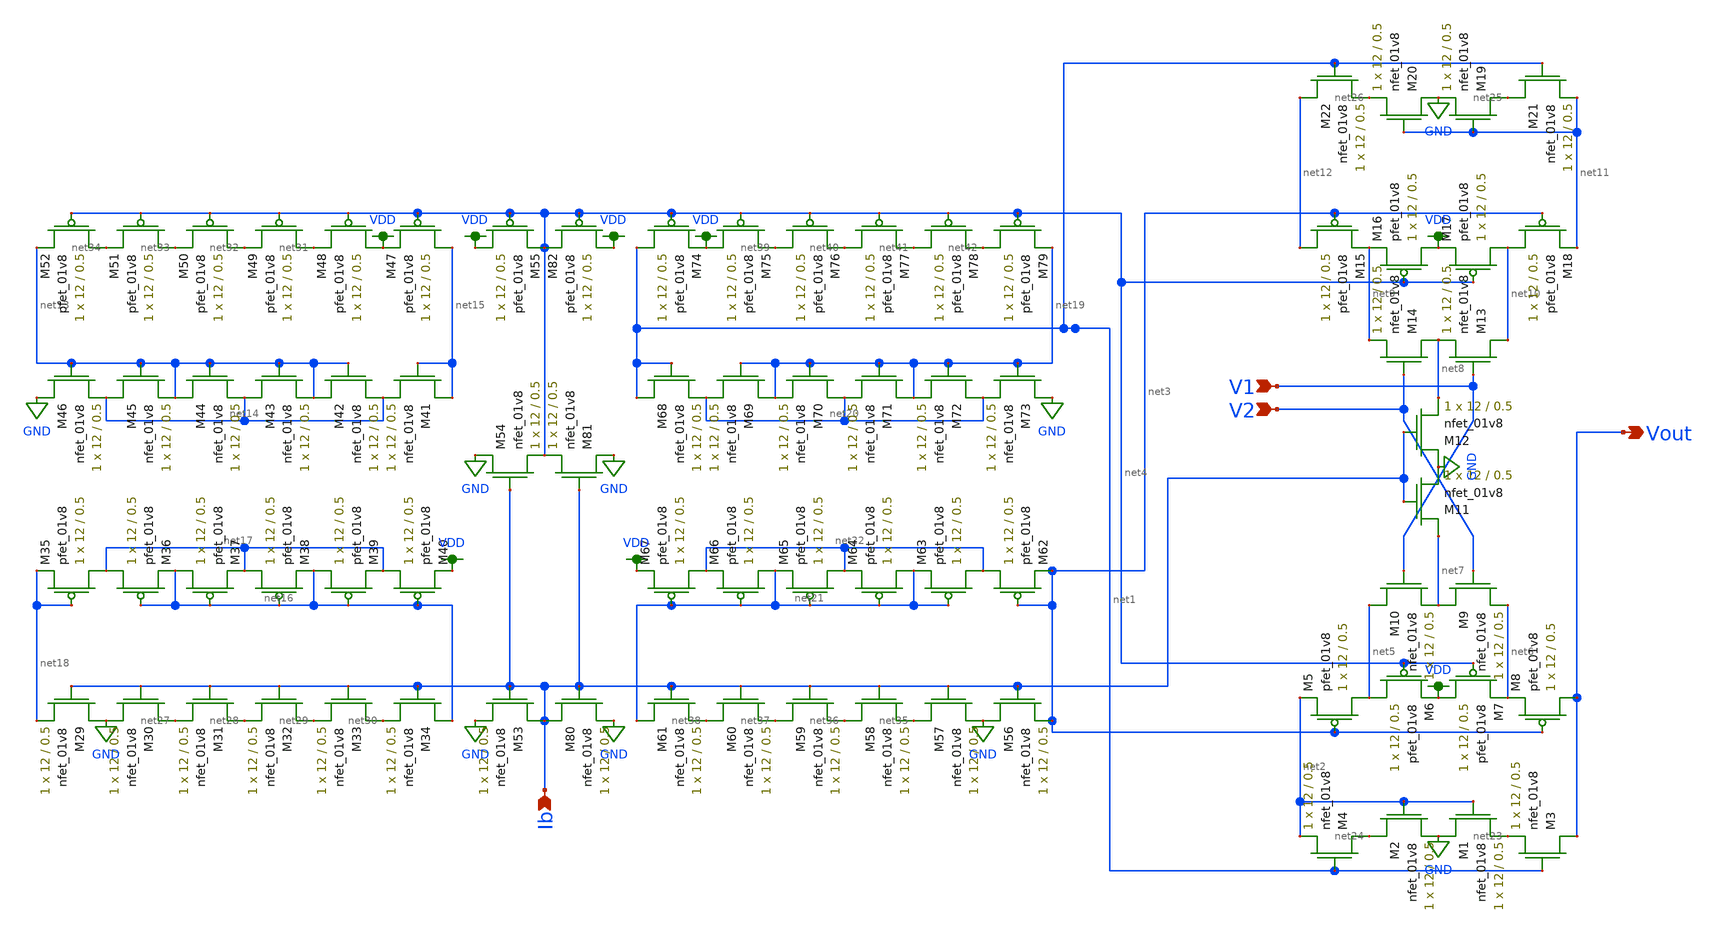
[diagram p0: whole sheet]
** sch_path: mp3/schematics/overall.sch
**.subckt overall V2 V1 Vout Ib
*.ipin V2
*.ipin V1
*.opin Vout
*.ipin Ib
XM1 GND net2 net23 GND sky130_fd_pr__nfet_01v8 L=0.5 W=12 nf=1 ad='int((nf+1)/2) * W/nf * 0.29' as='int((nf+2)/2) * W/nf * 0.29'
+ pd='2*int((nf+1)/2) * (W/nf + 0.29)' ps='2*int((nf+2)/2) * (W/nf + 0.29)' nrd='0.29 / W' nrs='0.29 / W'
+ sa=0 sb=0 sd=0 mult=1 m=1
XM2 net24 net2 GND GND sky130_fd_pr__nfet_01v8 L=0.5 W=12 nf=1 ad='int((nf+1)/2) * W/nf * 0.29' as='int((nf+2)/2) * W/nf * 0.29'
+ pd='2*int((nf+1)/2) * (W/nf + 0.29)' ps='2*int((nf+2)/2) * (W/nf + 0.29)' nrd='0.29 / W' nrs='0.29 / W'
+ sa=0 sb=0 sd=0 mult=1 m=1
XM3 Vout net1 net23 GND sky130_fd_pr__nfet_01v8 L=0.5 W=12 nf=1 ad='int((nf+1)/2) * W/nf * 0.29' as='int((nf+2)/2) * W/nf * 0.29'
+ pd='2*int((nf+1)/2) * (W/nf + 0.29)' ps='2*int((nf+2)/2) * (W/nf + 0.29)' nrd='0.29 / W' nrs='0.29 / W'
+ sa=0 sb=0 sd=0 mult=1 m=1
XM4 net24 net1 net2 GND sky130_fd_pr__nfet_01v8 L=0.5 W=12 nf=1 ad='int((nf+1)/2) * W/nf * 0.29' as='int((nf+2)/2) * W/nf * 0.29'
+ pd='2*int((nf+1)/2) * (W/nf + 0.29)' ps='2*int((nf+2)/2) * (W/nf + 0.29)' nrd='0.29 / W' nrs='0.29 / W'
+ sa=0 sb=0 sd=0 mult=1 m=1
XM5 net5 net3 net2 VDD sky130_fd_pr__pfet_01v8 L=0.5 W=12 nf=1 ad='int((nf+1)/2) * W/nf * 0.29' as='int((nf+2)/2) * W/nf * 0.29'
+ pd='2*int((nf+1)/2) * (W/nf + 0.29)' ps='2*int((nf+2)/2) * (W/nf + 0.29)' nrd='0.29 / W' nrs='0.29 / W'
+ sa=0 sb=0 sd=0 mult=1 m=1
XM6 net5 net4 VDD VDD sky130_fd_pr__pfet_01v8 L=0.5 W=12 nf=1 ad='int((nf+1)/2) * W/nf * 0.29' as='int((nf+2)/2) * W/nf * 0.29'
+ pd='2*int((nf+1)/2) * (W/nf + 0.29)' ps='2*int((nf+2)/2) * (W/nf + 0.29)' nrd='0.29 / W' nrs='0.29 / W'
+ sa=0 sb=0 sd=0 mult=1 m=1
XM7 VDD net4 net6 VDD sky130_fd_pr__pfet_01v8 L=0.5 W=12 nf=1 ad='int((nf+1)/2) * W/nf * 0.29' as='int((nf+2)/2) * W/nf * 0.29'
+ pd='2*int((nf+1)/2) * (W/nf + 0.29)' ps='2*int((nf+2)/2) * (W/nf + 0.29)' nrd='0.29 / W' nrs='0.29 / W'
+ sa=0 sb=0 sd=0 mult=1 m=1
XM8 Vout net3 net6 VDD sky130_fd_pr__pfet_01v8 L=0.5 W=12 nf=1 ad='int((nf+1)/2) * W/nf * 0.29' as='int((nf+2)/2) * W/nf * 0.29'
+ pd='2*int((nf+1)/2) * (W/nf + 0.29)' ps='2*int((nf+2)/2) * (W/nf + 0.29)' nrd='0.29 / W' nrs='0.29 / W'
+ sa=0 sb=0 sd=0 mult=1 m=1
XM9 net7 V2 net6 GND sky130_fd_pr__nfet_01v8 L=0.5 W=12 nf=1 ad='int((nf+1)/2) * W/nf * 0.29' as='int((nf+2)/2) * W/nf * 0.29'
+ pd='2*int((nf+1)/2) * (W/nf + 0.29)' ps='2*int((nf+2)/2) * (W/nf + 0.29)' nrd='0.29 / W' nrs='0.29 / W'
+ sa=0 sb=0 sd=0 mult=1 m=1
XM10 net5 V1 net7 GND sky130_fd_pr__nfet_01v8 L=0.5 W=12 nf=1 ad='int((nf+1)/2) * W/nf * 0.29' as='int((nf+2)/2) * W/nf * 0.29'
+ pd='2*int((nf+1)/2) * (W/nf + 0.29)' ps='2*int((nf+2)/2) * (W/nf + 0.29)' nrd='0.29 / W' nrs='0.29 / W'
+ sa=0 sb=0 sd=0 mult=1 m=1
XM11 net7 Ib GND GND sky130_fd_pr__nfet_01v8 L=0.5 W=12 nf=1 ad='int((nf+1)/2) * W/nf * 0.29' as='int((nf+2)/2) * W/nf * 0.29'
+ pd='2*int((nf+1)/2) * (W/nf + 0.29)' ps='2*int((nf+2)/2) * (W/nf + 0.29)' nrd='0.29 / W' nrs='0.29 / W'
+ sa=0 sb=0 sd=0 mult=1 m=1
XM12 GND Ib net8 GND sky130_fd_pr__nfet_01v8 L=0.5 W=12 nf=1 ad='int((nf+1)/2) * W/nf * 0.29' as='int((nf+2)/2) * W/nf * 0.29'
+ pd='2*int((nf+1)/2) * (W/nf + 0.29)' ps='2*int((nf+2)/2) * (W/nf + 0.29)' nrd='0.29 / W' nrs='0.29 / W'
+ sa=0 sb=0 sd=0 mult=1 m=1
XM13 net10 V1 net8 GND sky130_fd_pr__nfet_01v8 L=0.5 W=12 nf=1 ad='int((nf+1)/2) * W/nf * 0.29' as='int((nf+2)/2) * W/nf * 0.29'
+ pd='2*int((nf+1)/2) * (W/nf + 0.29)' ps='2*int((nf+2)/2) * (W/nf + 0.29)' nrd='0.29 / W' nrs='0.29 / W'
+ sa=0 sb=0 sd=0 mult=1 m=1
XM14 net8 V2 net9 GND sky130_fd_pr__nfet_01v8 L=0.5 W=12 nf=1 ad='int((nf+1)/2) * W/nf * 0.29' as='int((nf+2)/2) * W/nf * 0.29'
+ pd='2*int((nf+1)/2) * (W/nf + 0.29)' ps='2*int((nf+2)/2) * (W/nf + 0.29)' nrd='0.29 / W' nrs='0.29 / W'
+ sa=0 sb=0 sd=0 mult=1 m=1
XM15 net12 net3 net9 VDD sky130_fd_pr__pfet_01v8 L=0.5 W=12 nf=1 ad='int((nf+1)/2) * W/nf * 0.29' as='int((nf+2)/2) * W/nf * 0.29'
+ pd='2*int((nf+1)/2) * (W/nf + 0.29)' ps='2*int((nf+2)/2) * (W/nf + 0.29)' nrd='0.29 / W' nrs='0.29 / W'
+ sa=0 sb=0 sd=0 mult=1 m=1
XM16 VDD net4 net9 VDD sky130_fd_pr__pfet_01v8 L=0.5 W=12 nf=1 ad='int((nf+1)/2) * W/nf * 0.29' as='int((nf+2)/2) * W/nf * 0.29'
+ pd='2*int((nf+1)/2) * (W/nf + 0.29)' ps='2*int((nf+2)/2) * (W/nf + 0.29)' nrd='0.29 / W' nrs='0.29 / W'
+ sa=0 sb=0 sd=0 mult=1 m=1
XM17 net10 net4 VDD VDD sky130_fd_pr__pfet_01v8 L=0.5 W=12 nf=1 ad='int((nf+1)/2) * W/nf * 0.29' as='int((nf+2)/2) * W/nf * 0.29'
+ pd='2*int((nf+1)/2) * (W/nf + 0.29)' ps='2*int((nf+2)/2) * (W/nf + 0.29)' nrd='0.29 / W' nrs='0.29 / W'
+ sa=0 sb=0 sd=0 mult=1 m=1
XM18 net10 net3 net11 VDD sky130_fd_pr__pfet_01v8 L=0.5 W=12 nf=1 ad='int((nf+1)/2) * W/nf * 0.29' as='int((nf+2)/2) * W/nf * 0.29'
+ pd='2*int((nf+1)/2) * (W/nf + 0.29)' ps='2*int((nf+2)/2) * (W/nf + 0.29)' nrd='0.29 / W' nrs='0.29 / W'
+ sa=0 sb=0 sd=0 mult=1 m=1
XM19 net25 net11 GND GND sky130_fd_pr__nfet_01v8 L=0.5 W=12 nf=1 ad='int((nf+1)/2) * W/nf * 0.29' as='int((nf+2)/2) * W/nf * 0.29'
+ pd='2*int((nf+1)/2) * (W/nf + 0.29)' ps='2*int((nf+2)/2) * (W/nf + 0.29)' nrd='0.29 / W' nrs='0.29 / W'
+ sa=0 sb=0 sd=0 mult=1 m=1
XM20 GND net11 net26 GND sky130_fd_pr__nfet_01v8 L=0.5 W=12 nf=1 ad='int((nf+1)/2) * W/nf * 0.29' as='int((nf+2)/2) * W/nf * 0.29'
+ pd='2*int((nf+1)/2) * (W/nf + 0.29)' ps='2*int((nf+2)/2) * (W/nf + 0.29)' nrd='0.29 / W' nrs='0.29 / W'
+ sa=0 sb=0 sd=0 mult=1 m=1
XM21 net25 net1 net11 GND sky130_fd_pr__nfet_01v8 L=0.5 W=12 nf=1 ad='int((nf+1)/2) * W/nf * 0.29' as='int((nf+2)/2) * W/nf * 0.29'
+ pd='2*int((nf+1)/2) * (W/nf + 0.29)' ps='2*int((nf+2)/2) * (W/nf + 0.29)' nrd='0.29 / W' nrs='0.29 / W'
+ sa=0 sb=0 sd=0 mult=1 m=1
XM22 net12 net1 net26 GND sky130_fd_pr__nfet_01v8 L=0.5 W=12 nf=1 ad='int((nf+1)/2) * W/nf * 0.29' as='int((nf+2)/2) * W/nf * 0.29'
+ pd='2*int((nf+1)/2) * (W/nf + 0.29)' ps='2*int((nf+2)/2) * (W/nf + 0.29)' nrd='0.29 / W' nrs='0.29 / W'
+ sa=0 sb=0 sd=0 mult=1 m=1
XM29 GND Ib net18 GND sky130_fd_pr__nfet_01v8 L=0.5 W=12 nf=1 ad='int((nf+1)/2) * W/nf * 0.29' as='int((nf+2)/2) * W/nf * 0.29'
+ pd='2*int((nf+1)/2) * (W/nf + 0.29)' ps='2*int((nf+2)/2) * (W/nf + 0.29)' nrd='0.29 / W' nrs='0.29 / W'
+ sa=0 sb=0 sd=0 mult=1 m=1
XM30 net27 Ib GND GND sky130_fd_pr__nfet_01v8 L=0.5 W=12 nf=1 ad='int((nf+1)/2) * W/nf * 0.29' as='int((nf+2)/2) * W/nf * 0.29'
+ pd='2*int((nf+1)/2) * (W/nf + 0.29)' ps='2*int((nf+2)/2) * (W/nf + 0.29)' nrd='0.29 / W' nrs='0.29 / W'
+ sa=0 sb=0 sd=0 mult=1 m=1
XM31 net28 Ib net27 GND sky130_fd_pr__nfet_01v8 L=0.5 W=12 nf=1 ad='int((nf+1)/2) * W/nf * 0.29' as='int((nf+2)/2) * W/nf * 0.29'
+ pd='2*int((nf+1)/2) * (W/nf + 0.29)' ps='2*int((nf+2)/2) * (W/nf + 0.29)' nrd='0.29 / W' nrs='0.29 / W'
+ sa=0 sb=0 sd=0 mult=1 m=1
XM32 net29 Ib net28 GND sky130_fd_pr__nfet_01v8 L=0.5 W=12 nf=1 ad='int((nf+1)/2) * W/nf * 0.29' as='int((nf+2)/2) * W/nf * 0.29'
+ pd='2*int((nf+1)/2) * (W/nf + 0.29)' ps='2*int((nf+2)/2) * (W/nf + 0.29)' nrd='0.29 / W' nrs='0.29 / W'
+ sa=0 sb=0 sd=0 mult=1 m=1
XM33 net30 Ib net29 GND sky130_fd_pr__nfet_01v8 L=0.5 W=12 nf=1 ad='int((nf+1)/2) * W/nf * 0.29' as='int((nf+2)/2) * W/nf * 0.29'
+ pd='2*int((nf+1)/2) * (W/nf + 0.29)' ps='2*int((nf+2)/2) * (W/nf + 0.29)' nrd='0.29 / W' nrs='0.29 / W'
+ sa=0 sb=0 sd=0 mult=1 m=1
XM34 net16 Ib net30 GND sky130_fd_pr__nfet_01v8 L=0.5 W=12 nf=1 ad='int((nf+1)/2) * W/nf * 0.29' as='int((nf+2)/2) * W/nf * 0.29'
+ pd='2*int((nf+1)/2) * (W/nf + 0.29)' ps='2*int((nf+2)/2) * (W/nf + 0.29)' nrd='0.29 / W' nrs='0.29 / W'
+ sa=0 sb=0 sd=0 mult=1 m=1
XM35 net17 net18 net18 VDD sky130_fd_pr__pfet_01v8 L=0.5 W=12 nf=1 ad='int((nf+1)/2) * W/nf * 0.29' as='int((nf+2)/2) * W/nf * 0.29'
+ pd='2*int((nf+1)/2) * (W/nf + 0.29)' ps='2*int((nf+2)/2) * (W/nf + 0.29)' nrd='0.29 / W' nrs='0.29 / W'
+ sa=0 sb=0 sd=0 mult=1 m=1
XM36 net17 net16 net16 VDD sky130_fd_pr__pfet_01v8 L=0.5 W=12 nf=1 ad='int((nf+1)/2) * W/nf * 0.29' as='int((nf+2)/2) * W/nf * 0.29'
+ pd='2*int((nf+1)/2) * (W/nf + 0.29)' ps='2*int((nf+2)/2) * (W/nf + 0.29)' nrd='0.29 / W' nrs='0.29 / W'
+ sa=0 sb=0 sd=0 mult=1 m=1
XM37 net16 net16 net17 VDD sky130_fd_pr__pfet_01v8 L=0.5 W=12 nf=1 ad='int((nf+1)/2) * W/nf * 0.29' as='int((nf+2)/2) * W/nf * 0.29'
+ pd='2*int((nf+1)/2) * (W/nf + 0.29)' ps='2*int((nf+2)/2) * (W/nf + 0.29)' nrd='0.29 / W' nrs='0.29 / W'
+ sa=0 sb=0 sd=0 mult=1 m=1
XM38 net17 net16 net16 VDD sky130_fd_pr__pfet_01v8 L=0.5 W=12 nf=1 ad='int((nf+1)/2) * W/nf * 0.29' as='int((nf+2)/2) * W/nf * 0.29'
+ pd='2*int((nf+1)/2) * (W/nf + 0.29)' ps='2*int((nf+2)/2) * (W/nf + 0.29)' nrd='0.29 / W' nrs='0.29 / W'
+ sa=0 sb=0 sd=0 mult=1 m=1
XM39 net16 net16 net17 VDD sky130_fd_pr__pfet_01v8 L=0.5 W=12 nf=1 ad='int((nf+1)/2) * W/nf * 0.29' as='int((nf+2)/2) * W/nf * 0.29'
+ pd='2*int((nf+1)/2) * (W/nf + 0.29)' ps='2*int((nf+2)/2) * (W/nf + 0.29)' nrd='0.29 / W' nrs='0.29 / W'
+ sa=0 sb=0 sd=0 mult=1 m=1
XM40 net17 net16 VDD VDD sky130_fd_pr__pfet_01v8 L=0.5 W=12 nf=1 ad='int((nf+1)/2) * W/nf * 0.29' as='int((nf+2)/2) * W/nf * 0.29'
+ pd='2*int((nf+1)/2) * (W/nf + 0.29)' ps='2*int((nf+2)/2) * (W/nf + 0.29)' nrd='0.29 / W' nrs='0.29 / W'
+ sa=0 sb=0 sd=0 mult=1 m=1
XM41 net15 net15 net14 GND sky130_fd_pr__nfet_01v8 L=0.5 W=12 nf=1 ad='int((nf+1)/2) * W/nf * 0.29' as='int((nf+2)/2) * W/nf * 0.29'
+ pd='2*int((nf+1)/2) * (W/nf + 0.29)' ps='2*int((nf+2)/2) * (W/nf + 0.29)' nrd='0.29 / W' nrs='0.29 / W'
+ sa=0 sb=0 sd=0 mult=1 m=1
XM42 net13 net13 net14 GND sky130_fd_pr__nfet_01v8 L=0.5 W=12 nf=1 ad='int((nf+1)/2) * W/nf * 0.29' as='int((nf+2)/2) * W/nf * 0.29'
+ pd='2*int((nf+1)/2) * (W/nf + 0.29)' ps='2*int((nf+2)/2) * (W/nf + 0.29)' nrd='0.29 / W' nrs='0.29 / W'
+ sa=0 sb=0 sd=0 mult=1 m=1
XM43 net14 net13 net13 GND sky130_fd_pr__nfet_01v8 L=0.5 W=12 nf=1 ad='int((nf+1)/2) * W/nf * 0.29' as='int((nf+2)/2) * W/nf * 0.29'
+ pd='2*int((nf+1)/2) * (W/nf + 0.29)' ps='2*int((nf+2)/2) * (W/nf + 0.29)' nrd='0.29 / W' nrs='0.29 / W'
+ sa=0 sb=0 sd=0 mult=1 m=1
XM44 net13 net13 net14 GND sky130_fd_pr__nfet_01v8 L=0.5 W=12 nf=1 ad='int((nf+1)/2) * W/nf * 0.29' as='int((nf+2)/2) * W/nf * 0.29'
+ pd='2*int((nf+1)/2) * (W/nf + 0.29)' ps='2*int((nf+2)/2) * (W/nf + 0.29)' nrd='0.29 / W' nrs='0.29 / W'
+ sa=0 sb=0 sd=0 mult=1 m=1
XM45 net14 net13 net13 GND sky130_fd_pr__nfet_01v8 L=0.5 W=12 nf=1 ad='int((nf+1)/2) * W/nf * 0.29' as='int((nf+2)/2) * W/nf * 0.29'
+ pd='2*int((nf+1)/2) * (W/nf + 0.29)' ps='2*int((nf+2)/2) * (W/nf + 0.29)' nrd='0.29 / W' nrs='0.29 / W'
+ sa=0 sb=0 sd=0 mult=1 m=1
XM46 GND net13 net14 GND sky130_fd_pr__nfet_01v8 L=0.5 W=12 nf=1 ad='int((nf+1)/2) * W/nf * 0.29' as='int((nf+2)/2) * W/nf * 0.29'
+ pd='2*int((nf+1)/2) * (W/nf + 0.29)' ps='2*int((nf+2)/2) * (W/nf + 0.29)' nrd='0.29 / W' nrs='0.29 / W'
+ sa=0 sb=0 sd=0 mult=1 m=1
XM47 net15 net4 VDD VDD sky130_fd_pr__pfet_01v8 L=0.5 W=12 nf=1 ad='int((nf+1)/2) * W/nf * 0.29' as='int((nf+2)/2) * W/nf * 0.29'
+ pd='2*int((nf+1)/2) * (W/nf + 0.29)' ps='2*int((nf+2)/2) * (W/nf + 0.29)' nrd='0.29 / W' nrs='0.29 / W'
+ sa=0 sb=0 sd=0 mult=1 m=1
XM48 VDD net4 net31 VDD sky130_fd_pr__pfet_01v8 L=0.5 W=12 nf=1 ad='int((nf+1)/2) * W/nf * 0.29' as='int((nf+2)/2) * W/nf * 0.29'
+ pd='2*int((nf+1)/2) * (W/nf + 0.29)' ps='2*int((nf+2)/2) * (W/nf + 0.29)' nrd='0.29 / W' nrs='0.29 / W'
+ sa=0 sb=0 sd=0 mult=1 m=1
XM49 net31 net4 net32 VDD sky130_fd_pr__pfet_01v8 L=0.5 W=12 nf=1 ad='int((nf+1)/2) * W/nf * 0.29' as='int((nf+2)/2) * W/nf * 0.29'
+ pd='2*int((nf+1)/2) * (W/nf + 0.29)' ps='2*int((nf+2)/2) * (W/nf + 0.29)' nrd='0.29 / W' nrs='0.29 / W'
+ sa=0 sb=0 sd=0 mult=1 m=1
XM50 net32 net4 net33 VDD sky130_fd_pr__pfet_01v8 L=0.5 W=12 nf=1 ad='int((nf+1)/2) * W/nf * 0.29' as='int((nf+2)/2) * W/nf * 0.29'
+ pd='2*int((nf+1)/2) * (W/nf + 0.29)' ps='2*int((nf+2)/2) * (W/nf + 0.29)' nrd='0.29 / W' nrs='0.29 / W'
+ sa=0 sb=0 sd=0 mult=1 m=1
XM51 net33 net4 net34 VDD sky130_fd_pr__pfet_01v8 L=0.5 W=12 nf=1 ad='int((nf+1)/2) * W/nf * 0.29' as='int((nf+2)/2) * W/nf * 0.29'
+ pd='2*int((nf+1)/2) * (W/nf + 0.29)' ps='2*int((nf+2)/2) * (W/nf + 0.29)' nrd='0.29 / W' nrs='0.29 / W'
+ sa=0 sb=0 sd=0 mult=1 m=1
XM52 net34 net4 net13 VDD sky130_fd_pr__pfet_01v8 L=0.5 W=12 nf=1 ad='int((nf+1)/2) * W/nf * 0.29' as='int((nf+2)/2) * W/nf * 0.29'
+ pd='2*int((nf+1)/2) * (W/nf + 0.29)' ps='2*int((nf+2)/2) * (W/nf + 0.29)' nrd='0.29 / W' nrs='0.29 / W'
+ sa=0 sb=0 sd=0 mult=1 m=1
XM53 Ib Ib GND GND sky130_fd_pr__nfet_01v8 L=0.5 W=12 nf=1 ad='int((nf+1)/2) * W/nf * 0.29' as='int((nf+2)/2) * W/nf * 0.29'
+ pd='2*int((nf+1)/2) * (W/nf + 0.29)' ps='2*int((nf+2)/2) * (W/nf + 0.29)' nrd='0.29 / W' nrs='0.29 / W'
+ sa=0 sb=0 sd=0 mult=1 m=1
XM54 GND Ib net4 GND sky130_fd_pr__nfet_01v8 L=0.5 W=12 nf=1 ad='int((nf+1)/2) * W/nf * 0.29' as='int((nf+2)/2) * W/nf * 0.29'
+ pd='2*int((nf+1)/2) * (W/nf + 0.29)' ps='2*int((nf+2)/2) * (W/nf + 0.29)' nrd='0.29 / W' nrs='0.29 / W'
+ sa=0 sb=0 sd=0 mult=1 m=1
XM55 VDD net4 net4 VDD sky130_fd_pr__pfet_01v8 L=0.5 W=12 nf=1 ad='int((nf+1)/2) * W/nf * 0.29' as='int((nf+2)/2) * W/nf * 0.29'
+ pd='2*int((nf+1)/2) * (W/nf + 0.29)' ps='2*int((nf+2)/2) * (W/nf + 0.29)' nrd='0.29 / W' nrs='0.29 / W'
+ sa=0 sb=0 sd=0 mult=1 m=1
XM56 GND Ib net3 GND sky130_fd_pr__nfet_01v8 L=0.5 W=12 nf=1 ad='int((nf+1)/2) * W/nf * 0.29' as='int((nf+2)/2) * W/nf * 0.29'
+ pd='2*int((nf+1)/2) * (W/nf + 0.29)' ps='2*int((nf+2)/2) * (W/nf + 0.29)' nrd='0.29 / W' nrs='0.29 / W'
+ sa=0 sb=0 sd=0 mult=1 m=1
XM57 net35 Ib GND GND sky130_fd_pr__nfet_01v8 L=0.5 W=12 nf=1 ad='int((nf+1)/2) * W/nf * 0.29' as='int((nf+2)/2) * W/nf * 0.29'
+ pd='2*int((nf+1)/2) * (W/nf + 0.29)' ps='2*int((nf+2)/2) * (W/nf + 0.29)' nrd='0.29 / W' nrs='0.29 / W'
+ sa=0 sb=0 sd=0 mult=1 m=1
XM58 net36 Ib net35 GND sky130_fd_pr__nfet_01v8 L=0.5 W=12 nf=1 ad='int((nf+1)/2) * W/nf * 0.29' as='int((nf+2)/2) * W/nf * 0.29'
+ pd='2*int((nf+1)/2) * (W/nf + 0.29)' ps='2*int((nf+2)/2) * (W/nf + 0.29)' nrd='0.29 / W' nrs='0.29 / W'
+ sa=0 sb=0 sd=0 mult=1 m=1
XM59 net37 Ib net36 GND sky130_fd_pr__nfet_01v8 L=0.5 W=12 nf=1 ad='int((nf+1)/2) * W/nf * 0.29' as='int((nf+2)/2) * W/nf * 0.29'
+ pd='2*int((nf+1)/2) * (W/nf + 0.29)' ps='2*int((nf+2)/2) * (W/nf + 0.29)' nrd='0.29 / W' nrs='0.29 / W'
+ sa=0 sb=0 sd=0 mult=1 m=1
XM60 net38 Ib net37 GND sky130_fd_pr__nfet_01v8 L=0.5 W=12 nf=1 ad='int((nf+1)/2) * W/nf * 0.29' as='int((nf+2)/2) * W/nf * 0.29'
+ pd='2*int((nf+1)/2) * (W/nf + 0.29)' ps='2*int((nf+2)/2) * (W/nf + 0.29)' nrd='0.29 / W' nrs='0.29 / W'
+ sa=0 sb=0 sd=0 mult=1 m=1
XM61 net21 Ib net38 GND sky130_fd_pr__nfet_01v8 L=0.5 W=12 nf=1 ad='int((nf+1)/2) * W/nf * 0.29' as='int((nf+2)/2) * W/nf * 0.29'
+ pd='2*int((nf+1)/2) * (W/nf + 0.29)' ps='2*int((nf+2)/2) * (W/nf + 0.29)' nrd='0.29 / W' nrs='0.29 / W'
+ sa=0 sb=0 sd=0 mult=1 m=1
XM62 net22 net3 net3 VDD sky130_fd_pr__pfet_01v8 L=0.5 W=12 nf=1 ad='int((nf+1)/2) * W/nf * 0.29' as='int((nf+2)/2) * W/nf * 0.29'
+ pd='2*int((nf+1)/2) * (W/nf + 0.29)' ps='2*int((nf+2)/2) * (W/nf + 0.29)' nrd='0.29 / W' nrs='0.29 / W'
+ sa=0 sb=0 sd=0 mult=1 m=1
XM63 net22 net21 net21 VDD sky130_fd_pr__pfet_01v8 L=0.5 W=12 nf=1 ad='int((nf+1)/2) * W/nf * 0.29' as='int((nf+2)/2) * W/nf * 0.29'
+ pd='2*int((nf+1)/2) * (W/nf + 0.29)' ps='2*int((nf+2)/2) * (W/nf + 0.29)' nrd='0.29 / W' nrs='0.29 / W'
+ sa=0 sb=0 sd=0 mult=1 m=1
XM64 net21 net21 net22 VDD sky130_fd_pr__pfet_01v8 L=0.5 W=12 nf=1 ad='int((nf+1)/2) * W/nf * 0.29' as='int((nf+2)/2) * W/nf * 0.29'
+ pd='2*int((nf+1)/2) * (W/nf + 0.29)' ps='2*int((nf+2)/2) * (W/nf + 0.29)' nrd='0.29 / W' nrs='0.29 / W'
+ sa=0 sb=0 sd=0 mult=1 m=1
XM65 net22 net21 net21 VDD sky130_fd_pr__pfet_01v8 L=0.5 W=12 nf=1 ad='int((nf+1)/2) * W/nf * 0.29' as='int((nf+2)/2) * W/nf * 0.29'
+ pd='2*int((nf+1)/2) * (W/nf + 0.29)' ps='2*int((nf+2)/2) * (W/nf + 0.29)' nrd='0.29 / W' nrs='0.29 / W'
+ sa=0 sb=0 sd=0 mult=1 m=1
XM66 net21 net21 net22 VDD sky130_fd_pr__pfet_01v8 L=0.5 W=12 nf=1 ad='int((nf+1)/2) * W/nf * 0.29' as='int((nf+2)/2) * W/nf * 0.29'
+ pd='2*int((nf+1)/2) * (W/nf + 0.29)' ps='2*int((nf+2)/2) * (W/nf + 0.29)' nrd='0.29 / W' nrs='0.29 / W'
+ sa=0 sb=0 sd=0 mult=1 m=1
XM67 net22 net21 VDD VDD sky130_fd_pr__pfet_01v8 L=0.5 W=12 nf=1 ad='int((nf+1)/2) * W/nf * 0.29' as='int((nf+2)/2) * W/nf * 0.29'
+ pd='2*int((nf+1)/2) * (W/nf + 0.29)' ps='2*int((nf+2)/2) * (W/nf + 0.29)' nrd='0.29 / W' nrs='0.29 / W'
+ sa=0 sb=0 sd=0 mult=1 m=1
XM68 net1 net1 net20 GND sky130_fd_pr__nfet_01v8 L=0.5 W=12 nf=1 ad='int((nf+1)/2) * W/nf * 0.29' as='int((nf+2)/2) * W/nf * 0.29'
+ pd='2*int((nf+1)/2) * (W/nf + 0.29)' ps='2*int((nf+2)/2) * (W/nf + 0.29)' nrd='0.29 / W' nrs='0.29 / W'
+ sa=0 sb=0 sd=0 mult=1 m=1
XM69 net19 net19 net20 GND sky130_fd_pr__nfet_01v8 L=0.5 W=12 nf=1 ad='int((nf+1)/2) * W/nf * 0.29' as='int((nf+2)/2) * W/nf * 0.29'
+ pd='2*int((nf+1)/2) * (W/nf + 0.29)' ps='2*int((nf+2)/2) * (W/nf + 0.29)' nrd='0.29 / W' nrs='0.29 / W'
+ sa=0 sb=0 sd=0 mult=1 m=1
XM70 net20 net19 net19 GND sky130_fd_pr__nfet_01v8 L=0.5 W=12 nf=1 ad='int((nf+1)/2) * W/nf * 0.29' as='int((nf+2)/2) * W/nf * 0.29'
+ pd='2*int((nf+1)/2) * (W/nf + 0.29)' ps='2*int((nf+2)/2) * (W/nf + 0.29)' nrd='0.29 / W' nrs='0.29 / W'
+ sa=0 sb=0 sd=0 mult=1 m=1
XM71 net19 net19 net20 GND sky130_fd_pr__nfet_01v8 L=0.5 W=12 nf=1 ad='int((nf+1)/2) * W/nf * 0.29' as='int((nf+2)/2) * W/nf * 0.29'
+ pd='2*int((nf+1)/2) * (W/nf + 0.29)' ps='2*int((nf+2)/2) * (W/nf + 0.29)' nrd='0.29 / W' nrs='0.29 / W'
+ sa=0 sb=0 sd=0 mult=1 m=1
XM72 net20 net19 net19 GND sky130_fd_pr__nfet_01v8 L=0.5 W=12 nf=1 ad='int((nf+1)/2) * W/nf * 0.29' as='int((nf+2)/2) * W/nf * 0.29'
+ pd='2*int((nf+1)/2) * (W/nf + 0.29)' ps='2*int((nf+2)/2) * (W/nf + 0.29)' nrd='0.29 / W' nrs='0.29 / W'
+ sa=0 sb=0 sd=0 mult=1 m=1
XM73 GND net19 net20 GND sky130_fd_pr__nfet_01v8 L=0.5 W=12 nf=1 ad='int((nf+1)/2) * W/nf * 0.29' as='int((nf+2)/2) * W/nf * 0.29'
+ pd='2*int((nf+1)/2) * (W/nf + 0.29)' ps='2*int((nf+2)/2) * (W/nf + 0.29)' nrd='0.29 / W' nrs='0.29 / W'
+ sa=0 sb=0 sd=0 mult=1 m=1
XM74 net1 net4 VDD VDD sky130_fd_pr__pfet_01v8 L=0.5 W=12 nf=1 ad='int((nf+1)/2) * W/nf * 0.29' as='int((nf+2)/2) * W/nf * 0.29'
+ pd='2*int((nf+1)/2) * (W/nf + 0.29)' ps='2*int((nf+2)/2) * (W/nf + 0.29)' nrd='0.29 / W' nrs='0.29 / W'
+ sa=0 sb=0 sd=0 mult=1 m=1
XM75 VDD net4 net39 VDD sky130_fd_pr__pfet_01v8 L=0.5 W=12 nf=1 ad='int((nf+1)/2) * W/nf * 0.29' as='int((nf+2)/2) * W/nf * 0.29'
+ pd='2*int((nf+1)/2) * (W/nf + 0.29)' ps='2*int((nf+2)/2) * (W/nf + 0.29)' nrd='0.29 / W' nrs='0.29 / W'
+ sa=0 sb=0 sd=0 mult=1 m=1
XM76 net39 net4 net40 VDD sky130_fd_pr__pfet_01v8 L=0.5 W=12 nf=1 ad='int((nf+1)/2) * W/nf * 0.29' as='int((nf+2)/2) * W/nf * 0.29'
+ pd='2*int((nf+1)/2) * (W/nf + 0.29)' ps='2*int((nf+2)/2) * (W/nf + 0.29)' nrd='0.29 / W' nrs='0.29 / W'
+ sa=0 sb=0 sd=0 mult=1 m=1
XM77 net40 net4 net41 VDD sky130_fd_pr__pfet_01v8 L=0.5 W=12 nf=1 ad='int((nf+1)/2) * W/nf * 0.29' as='int((nf+2)/2) * W/nf * 0.29'
+ pd='2*int((nf+1)/2) * (W/nf + 0.29)' ps='2*int((nf+2)/2) * (W/nf + 0.29)' nrd='0.29 / W' nrs='0.29 / W'
+ sa=0 sb=0 sd=0 mult=1 m=1
XM78 net41 net4 net42 VDD sky130_fd_pr__pfet_01v8 L=0.5 W=12 nf=1 ad='int((nf+1)/2) * W/nf * 0.29' as='int((nf+2)/2) * W/nf * 0.29'
+ pd='2*int((nf+1)/2) * (W/nf + 0.29)' ps='2*int((nf+2)/2) * (W/nf + 0.29)' nrd='0.29 / W' nrs='0.29 / W'
+ sa=0 sb=0 sd=0 mult=1 m=1
XM79 net42 net4 net19 VDD sky130_fd_pr__pfet_01v8 L=0.5 W=12 nf=1 ad='int((nf+1)/2) * W/nf * 0.29' as='int((nf+2)/2) * W/nf * 0.29'
+ pd='2*int((nf+1)/2) * (W/nf + 0.29)' ps='2*int((nf+2)/2) * (W/nf + 0.29)' nrd='0.29 / W' nrs='0.29 / W'
+ sa=0 sb=0 sd=0 mult=1 m=1
XM80 Ib Ib GND GND sky130_fd_pr__nfet_01v8 L=0.5 W=12 nf=1 ad='int((nf+1)/2) * W/nf * 0.29' as='int((nf+2)/2) * W/nf * 0.29'
+ pd='2*int((nf+1)/2) * (W/nf + 0.29)' ps='2*int((nf+2)/2) * (W/nf + 0.29)' nrd='0.29 / W' nrs='0.29 / W'
+ sa=0 sb=0 sd=0 mult=1 m=1
XM81 GND Ib net4 GND sky130_fd_pr__nfet_01v8 L=0.5 W=12 nf=1 ad='int((nf+1)/2) * W/nf * 0.29' as='int((nf+2)/2) * W/nf * 0.29'
+ pd='2*int((nf+1)/2) * (W/nf + 0.29)' ps='2*int((nf+2)/2) * (W/nf + 0.29)' nrd='0.29 / W' nrs='0.29 / W'
+ sa=0 sb=0 sd=0 mult=1 m=1
XM82 VDD net4 net4 VDD sky130_fd_pr__pfet_01v8 L=0.5 W=12 nf=1 ad='int((nf+1)/2) * W/nf * 0.29' as='int((nf+2)/2) * W/nf * 0.29'
+ pd='2*int((nf+1)/2) * (W/nf + 0.29)' ps='2*int((nf+2)/2) * (W/nf + 0.29)' nrd='0.29 / W' nrs='0.29 / W'
+ sa=0 sb=0 sd=0 mult=1 m=1
**.ends
.GLOBAL GND
.GLOBAL VDD
.end
